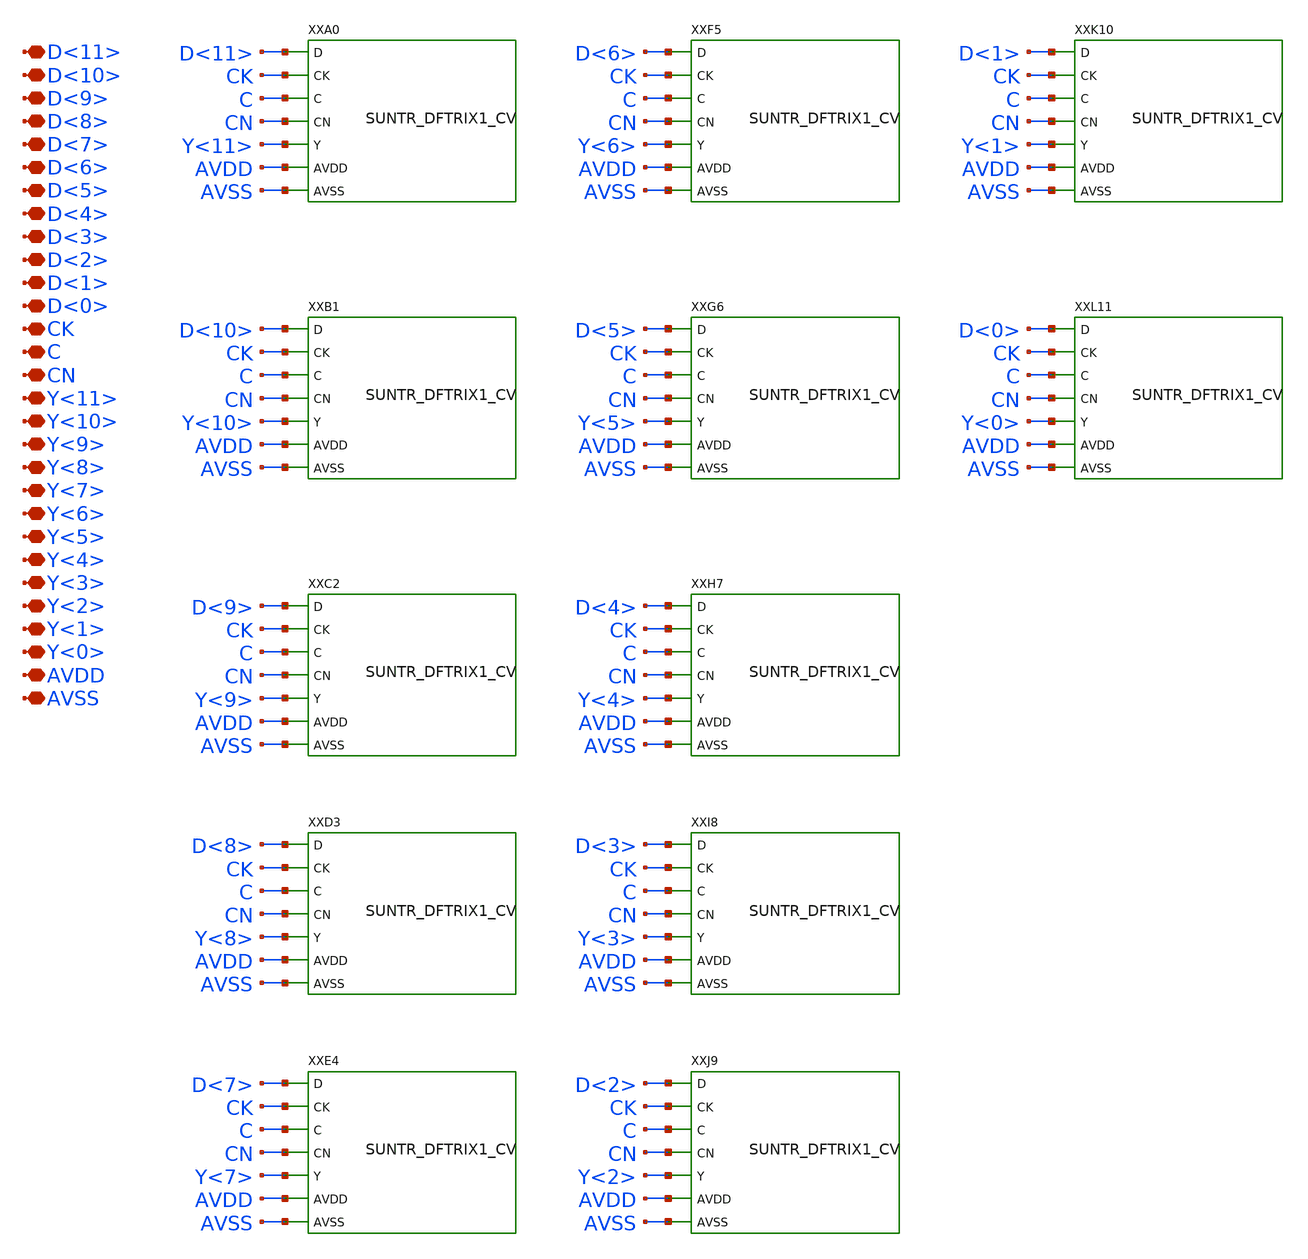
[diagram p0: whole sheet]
** sch_path: ip/sun_tr_sky130nm/design/SUN_TR_SKY130NM/SUNTR_RG12TRIX1_CV.sch
**.subckt SUNTR_RG12TRIX1_CV D<11> D<10> D<9> D<8> D<7> D<6> D<5> D<4> D<3> D<2> D<1> D<0> CK C CN
*+ Y<11> Y<10> Y<9> Y<8> Y<7> Y<6> Y<5> Y<4> Y<3> Y<2> Y<1> Y<0> AVDD AVSS
*.iopin D<11>
*.iopin D<10>
*.iopin D<9>
*.iopin D<8>
*.iopin D<7>
*.iopin D<6>
*.iopin D<5>
*.iopin D<4>
*.iopin D<3>
*.iopin D<2>
*.iopin D<1>
*.iopin D<0>
*.iopin CK
*.iopin C
*.iopin CN
*.iopin Y<11>
*.iopin Y<10>
*.iopin Y<9>
*.iopin Y<8>
*.iopin Y<7>
*.iopin Y<6>
*.iopin Y<5>
*.iopin Y<4>
*.iopin Y<3>
*.iopin Y<2>
*.iopin Y<1>
*.iopin Y<0>
*.iopin AVDD
*.iopin AVSS
XXA0 D<11> CK C CN Y<11> AVDD AVSS SUNTR_DFTRIX1_CV xoffset=0 yoffset=0 angle=0 M=1
XXB1 D<10> CK C CN Y<10> AVDD AVSS SUNTR_DFTRIX1_CV xoffset=0 yoffset=0 angle=0 M=1
XXC2 D<9> CK C CN Y<9> AVDD AVSS SUNTR_DFTRIX1_CV xoffset=0 yoffset=0 angle=0 M=1
XXD3 D<8> CK C CN Y<8> AVDD AVSS SUNTR_DFTRIX1_CV xoffset=0 yoffset=0 angle=0 M=1
XXE4 D<7> CK C CN Y<7> AVDD AVSS SUNTR_DFTRIX1_CV xoffset=0 yoffset=0 angle=0 M=1
XXF5 D<6> CK C CN Y<6> AVDD AVSS SUNTR_DFTRIX1_CV xoffset=0 yoffset=0 angle=0 M=1
XXG6 D<5> CK C CN Y<5> AVDD AVSS SUNTR_DFTRIX1_CV xoffset=0 yoffset=0 angle=0 M=1
XXH7 D<4> CK C CN Y<4> AVDD AVSS SUNTR_DFTRIX1_CV xoffset=0 yoffset=0 angle=0 M=1
XXI8 D<3> CK C CN Y<3> AVDD AVSS SUNTR_DFTRIX1_CV xoffset=0 yoffset=0 angle=0 M=1
XXJ9 D<2> CK C CN Y<2> AVDD AVSS SUNTR_DFTRIX1_CV xoffset=0 yoffset=0 angle=0 M=1
XXK10 D<1> CK C CN Y<1> AVDD AVSS SUNTR_DFTRIX1_CV xoffset=0 yoffset=0 angle=0 M=1
XXL11 D<0> CK C CN Y<0> AVDD AVSS SUNTR_DFTRIX1_CV xoffset=0 yoffset=0 angle=0 M=1
**.ends
.end
